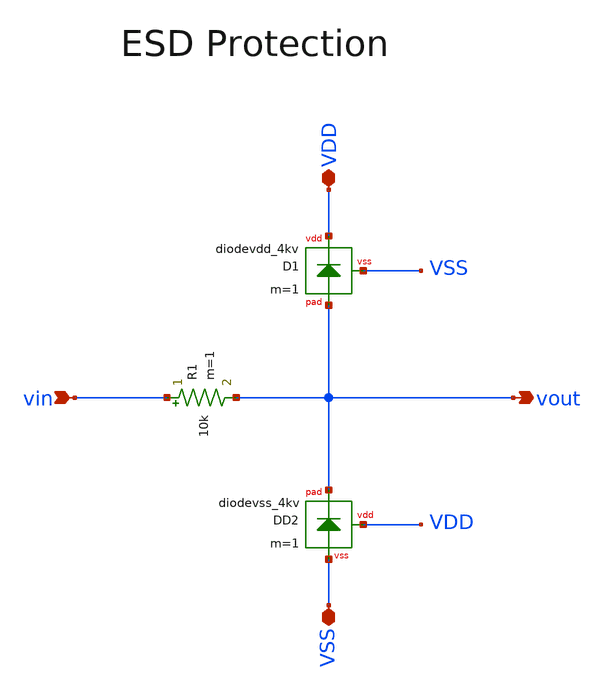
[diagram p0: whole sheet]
** sch_path: SG13G2_ATBS-ADC-main/xschem/top_level/auxiliary/esd_protection.sch
**.subckt esd_protection VDD VSS vin vout
*.iopin VDD
*.iopin VSS
*.ipin vin
*.opin vout
R1 vin vout 10k m=1
XD1 VDD vout VSS diodevdd_4kv m=1
XD2 VDD vout VSS diodevss_4kv m=1
**.ends
.end
